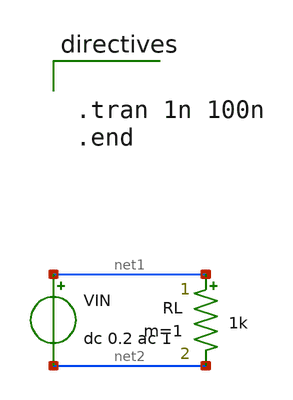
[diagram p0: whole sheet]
** sch_path: platform/packages/spicexplorer-netlist2xschem/tests/fixtures/xvport/tb_code_shown.sch
**.subckt tb_code_shown
VIN net1 net2 dc 0.2 ac 1
RL net1 net2 1k m=1
**** begin user architecture code


.tran 1n 100n
.end


**** end user architecture code
**.ends
.end
